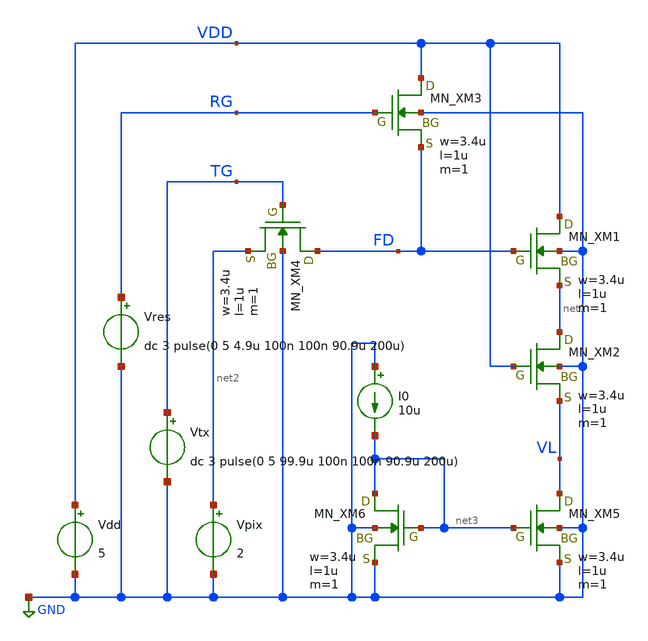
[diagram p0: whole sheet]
** sch_path: member_project/imager/YuMaehashi/design/tb_pixsf.sch
**.subckt tb_pixsf
XXM1 VDD FD net1 GND NMOS w=3.4u l=1u nrd=0 nrs=0 m=1
XXM2 net1 VDD VL GND NMOS w=3.4u l=1u nrd=0 nrs=0 m=1
XXM3 VDD RG FD GND NMOS w=3.4u l=1u nrd=0 nrs=0 m=1
XXM4 FD TG net2 GND NMOS w=3.4u l=1u nrd=0 nrs=0 m=1
XXM5 VL net3 GND GND NMOS w=3.4u l=1u nrd=0 nrs=0 m=1
XXM6 net3 net3 GND GND NMOS w=3.4u l=1u nrd=0 nrs=0 m=1
I0 GND net3 10u
Vpix net2 GND 2
Vtx TG GND dc 3 pulse(0 5 99.9u 100n 100n 90.9u 200u)
Vres RG GND dc 3 pulse(0 5 4.9u 100n 100n 90.9u 200u)
Vdd VDD GND 5
**** begin user architecture code


.option savecurrents
.control
set units=degree
save all

tran 10n 200u
write tb_pixsf.raw
.endc

 .include $::LIB/ip62_models
**** end user architecture code
**.ends
.GLOBAL GND
.end
